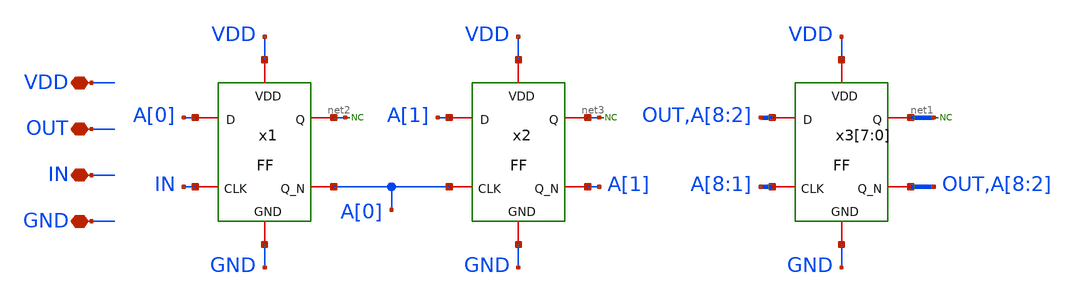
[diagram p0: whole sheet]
** sch_path: DIV/DIV.sch
**.subckt DIV GND IN VDD OUT
*.iopin GND
*.iopin IN
*.iopin VDD
*.iopin OUT
x1 VDD A[0] A[0] net2 IN GND FF
* noconn #net2
x2 VDD A[1] A[1] net3 A[0] GND FF
* noconn #net3
x3[7] VDD OUT OUT net1[7] A[8] GND FF
x3[6] VDD A[8] A[8] net1[6] A[7] GND FF
x3[5] VDD A[7] A[7] net1[5] A[6] GND FF
x3[4] VDD A[6] A[6] net1[4] A[5] GND FF
x3[3] VDD A[5] A[5] net1[3] A[4] GND FF
x3[2] VDD A[4] A[4] net1[2] A[3] GND FF
x3[1] VDD A[3] A[3] net1[1] A[2] GND FF
x3[0] VDD A[2] A[2] net1[0] A[1] GND FF
* noconn #net1
**.ends
.end
